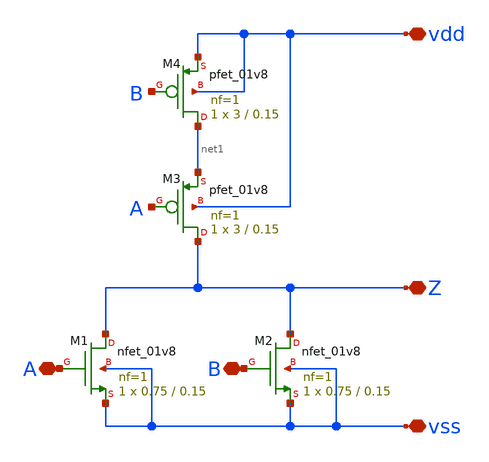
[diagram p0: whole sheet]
** sch_path: designs/sch/nor.sch
**.subckt nor A B vdd Z vss
*.iopin A
*.iopin B
*.iopin vdd
*.iopin Z
*.iopin vss
XM1 Z A vss vss sky130_fd_pr__nfet_01v8 L=0.15 W=0.75 nf=1 ad='int((nf+1)/2) * W/nf * 0.29' as='int((nf+2)/2) * W/nf * 0.29'
+ pd='2*int((nf+1)/2) * (W/nf + 0.29)' ps='2*int((nf+2)/2) * (W/nf + 0.29)' nrd='0.29 / W' nrs='0.29 / W'
+ sa=0 sb=0 sd=0 mult=1 m=1
XM4 net1 B vdd vdd sky130_fd_pr__pfet_01v8 L=0.15 W=3 nf=1 ad='int((nf+1)/2) * W/nf * 0.29' as='int((nf+2)/2) * W/nf * 0.29'
+ pd='2*int((nf+1)/2) * (W/nf + 0.29)' ps='2*int((nf+2)/2) * (W/nf + 0.29)' nrd='0.29 / W' nrs='0.29 / W'
+ sa=0 sb=0 sd=0 mult=1 m=1
XM2 Z B vss vss sky130_fd_pr__nfet_01v8 L=0.15 W=0.75 nf=1 ad='int((nf+1)/2) * W/nf * 0.29' as='int((nf+2)/2) * W/nf * 0.29'
+ pd='2*int((nf+1)/2) * (W/nf + 0.29)' ps='2*int((nf+2)/2) * (W/nf + 0.29)' nrd='0.29 / W' nrs='0.29 / W'
+ sa=0 sb=0 sd=0 mult=1 m=1
XM3 Z A net1 vdd sky130_fd_pr__pfet_01v8 L=0.15 W=3 nf=1 ad='int((nf+1)/2) * W/nf * 0.29' as='int((nf+2)/2) * W/nf * 0.29'
+ pd='2*int((nf+1)/2) * (W/nf + 0.29)' ps='2*int((nf+2)/2) * (W/nf + 0.29)' nrd='0.29 / W' nrs='0.29 / W'
+ sa=0 sb=0 sd=0 mult=1 m=1
**.ends
.end
